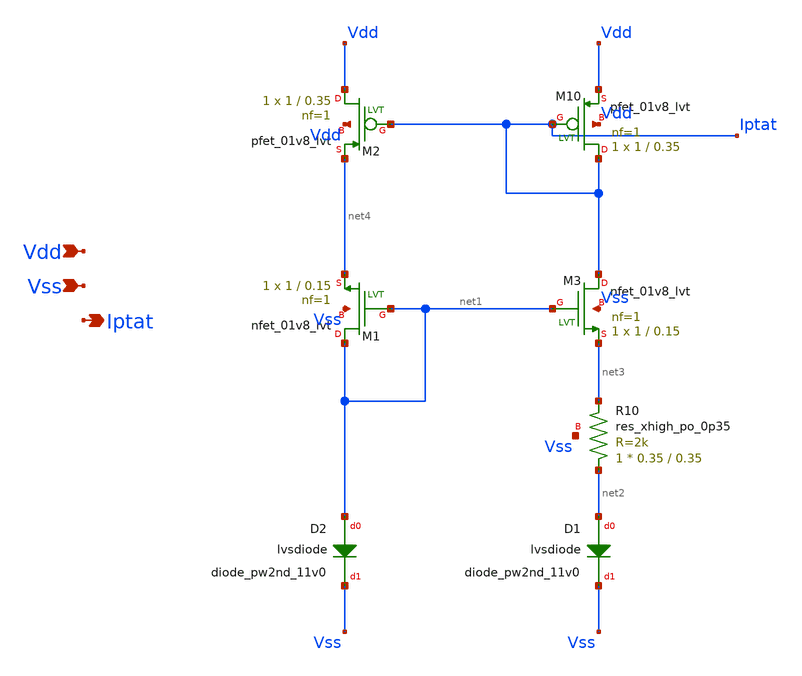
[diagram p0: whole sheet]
** sch_path: custom_gds/tt_um_test_commit/xschem/PTAT_wulff.sch
**.subckt PTAT_wulff Vdd Vss Iptat
*.ipin Vdd
*.ipin Vss
*.opin Iptat
XM10 Iptat Iptat Vdd Vdd sky130_fd_pr__pfet_01v8_lvt L=0.35 W=1 nf=1 ad='int((1 + 1)/2) * 1 / 1 * 0.29'
+ as='int((1 + 2)/2) * 1 / 1 * 0.29' pd='2*int((1 + 1)/2) * (1 / 1 + 0.29)' ps='2*int((1 + 2)/2) * (1 / 1 + 0.29)'
+ nrd='0.29 / 1 ' nrs='0.29 / 1 ' sa=0 sb=0 sd=0 mult=1 m=1
XM1 net1 net1 net4 Vss sky130_fd_pr__nfet_01v8_lvt L=0.15 W=1 nf=1 ad='int((1 + 1)/2) * 1 / 1 * 0.29'
+ as='int((1 + 2)/2) * 1 / 1 * 0.29' pd='2*int((1 + 1)/2) * (1 / 1 + 0.29)' ps='2*int((1 + 2)/2) * (1 / 1 + 0.29)'
+ nrd='0.29 / 1 ' nrs='0.29 / 1 ' sa=0 sb=0 sd=0 mult=1 m=1
XR10 net2 net3 Vss sky130_fd_pr__res_xhigh_po_0p35 L=0.35 mult=1 m=1
D2 net1 Vss sky130_fd_pr__diode_pw2nd_11v0 area=1e12
D1 net2 Vss sky130_fd_pr__diode_pw2nd_11v0 area=1e12
XM2 Vdd Iptat net4 Vdd sky130_fd_pr__pfet_01v8_lvt L=0.35 W=1 nf=1 ad='int((1 + 1)/2) * 1 / 1 * 0.29'
+ as='int((1 + 2)/2) * 1 / 1 * 0.29' pd='2*int((1 + 1)/2) * (1 / 1 + 0.29)' ps='2*int((1 + 2)/2) * (1 / 1 + 0.29)'
+ nrd='0.29 / 1 ' nrs='0.29 / 1 ' sa=0 sb=0 sd=0 mult=1 m=1
XM3 Iptat net1 net3 Vss sky130_fd_pr__nfet_01v8_lvt L=0.15 W=1 nf=1 ad='int((1 + 1)/2) * 1 / 1 * 0.29'
+ as='int((1 + 2)/2) * 1 / 1 * 0.29' pd='2*int((1 + 1)/2) * (1 / 1 + 0.29)' ps='2*int((1 + 2)/2) * (1 / 1 + 0.29)'
+ nrd='0.29 / 1 ' nrs='0.29 / 1 ' sa=0 sb=0 sd=0 mult=1 m=1
**.ends
.end
